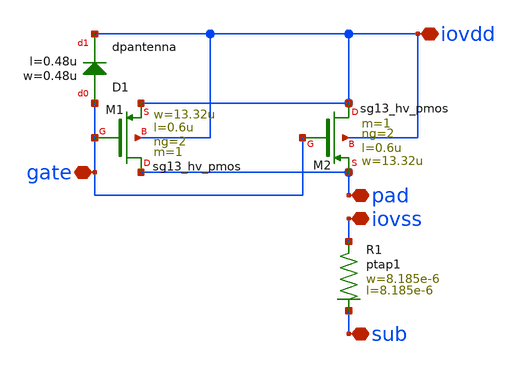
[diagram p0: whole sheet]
** sch_path: MSPHY6034-main/schematic/xschem/openpdk-libraries/ihp-sg13g2/sg13g2_io/xschem/sg13g2_Clamp_P2N2D.sch
**.subckt sg13g2_Clamp_P2N2D iovss gate pad iovdd sub
*.iopin iovss
*.iopin gate
*.iopin pad
*.iopin iovdd
*.iopin sub
XR1 iovss sub ptap1 R=9.826 w=8.185e-6 l=8.185e-6
XM1 pad gate iovdd iovdd sg13_hv_pmos w=13.32u l=0.6u ng=2 m=1 mm_ok=1
XM2 iovdd gate pad iovdd sg13_hv_pmos w=13.32u l=0.6u ng=2 m=1 mm_ok=1
XD1 gate iovdd dpantenna l=0.48u w=0.48u
**.ends
.end
